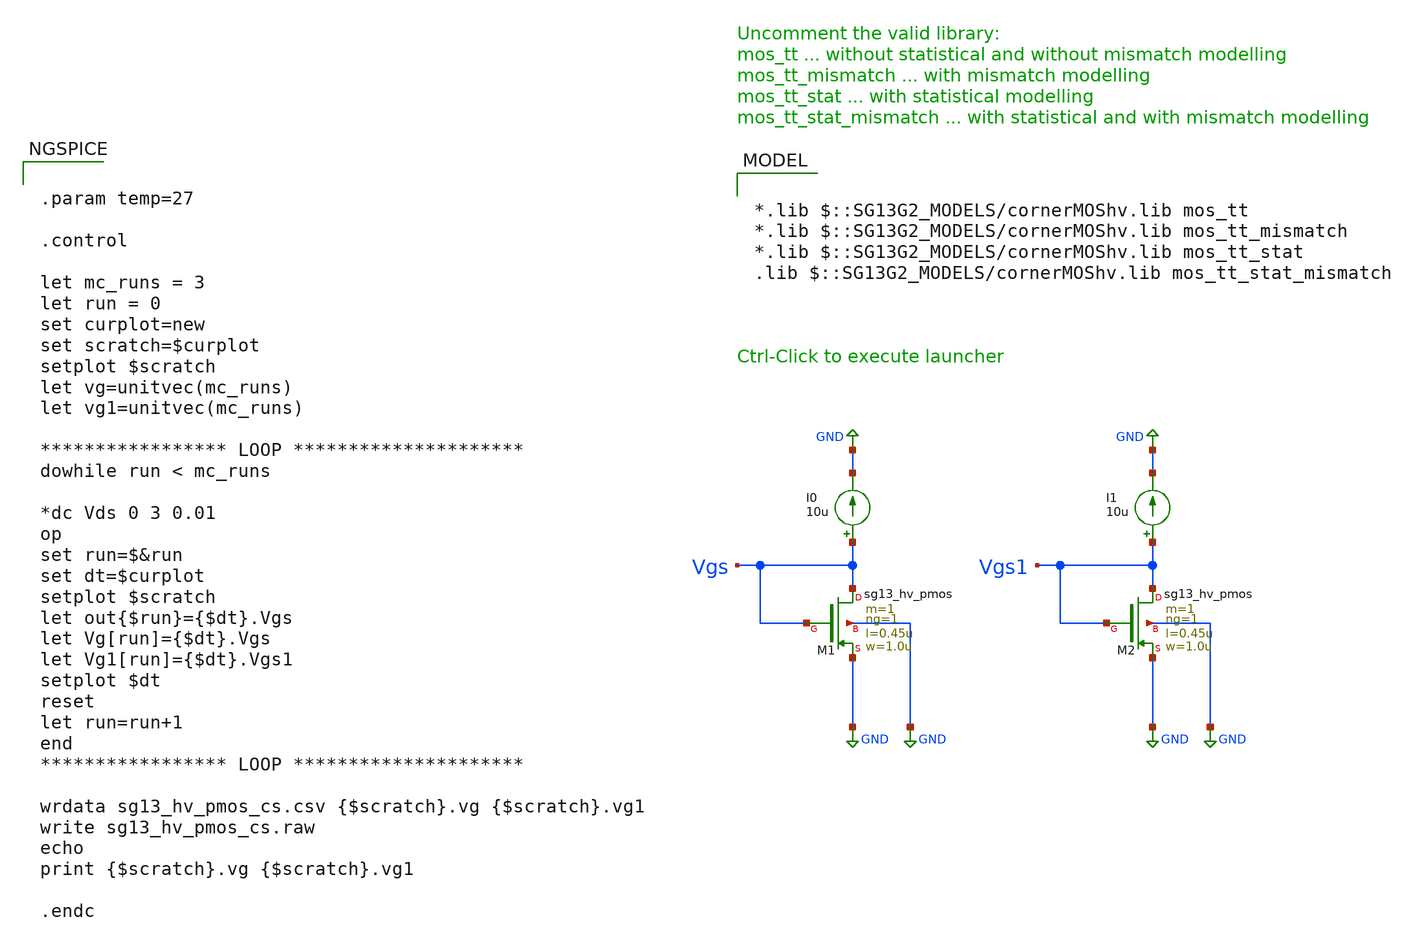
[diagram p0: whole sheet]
** sch_path: ihp-sg13g2/libs.tech/xschem/sg13g2_tests/mc_hv_pmos_cs_loop.sch
* Copyright 2023 IHP PDK Authors
**.subckt mc_hv_pmos_cs_loop
I0 Vgs GND 10u
XM1 Vgs Vgs GND GND sg13_hv_pmos w=1.0u l=0.45u ng=1 m=1 mm_ok=1
I1 Vgs1 GND 10u
XM2 Vgs1 Vgs1 GND GND sg13_hv_pmos w=1.0u l=0.45u ng=1 m=1 mm_ok=1
**** begin user architecture code


.param temp=27

.control

let mc_runs = 3
let run = 0
set curplot=new
set scratch=$curplot
setplot $scratch
let vg=unitvec(mc_runs)
let vg1=unitvec(mc_runs)

***************** LOOP *********************
dowhile run < mc_runs

*dc Vds 0 3 0.01
op
set run=$&run
set dt=$curplot
setplot $scratch
let out{$run}={$dt}.Vgs
let Vg[run]={$dt}.Vgs
let Vg1[run]={$dt}.Vgs1
setplot $dt
reset
let run=run+1
end
***************** LOOP *********************

wrdata sg13_hv_pmos_cs.csv {$scratch}.vg {$scratch}.vg1
write sg13_hv_pmos_cs.raw
echo
print {$scratch}.vg {$scratch}.vg1

.endc



*.lib $::SG13G2_MODELS/cornerMOShv.lib mos_tt
*.lib $::SG13G2_MODELS/cornerMOShv.lib mos_tt_mismatch
*.lib $::SG13G2_MODELS/cornerMOShv.lib mos_tt_stat
.lib $::SG13G2_MODELS/cornerMOShv.lib mos_tt_stat_mismatch

**** end user architecture code
**.ends
.GLOBAL GND
.end
